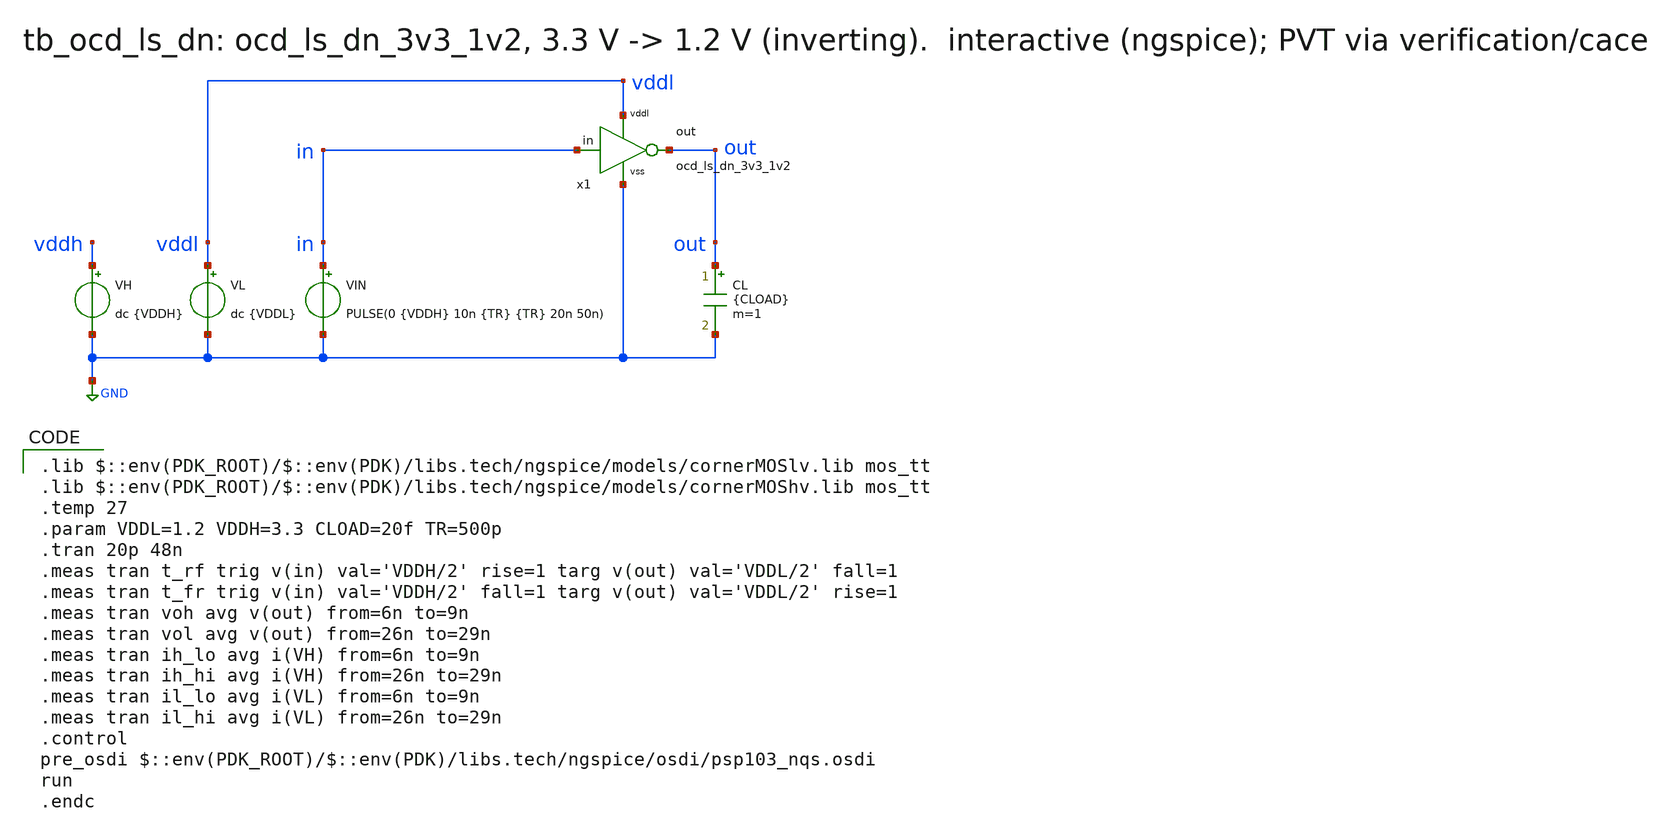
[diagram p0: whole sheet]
** sch_path: macros/ocd_ls_dn_3v3_1v2/testbenches/xschem/tb_ocd_ls_dn.sch
* macros/ocd_ls_dn_3v3_1v2/schematic/xschem/ocd_ls_dn_3v3_1v2.sym:
* Copyright 2023 IHP PDK Authors, Apache License 2.0 (https://www.apache.org/licenses/LICENSE-2.0)
**.subckt tb_ocd_ls_dn
x1 GND vddl out in ocd_ls_dn_3v3_1v2
VL vddl GND dc {VDDL}
VH vddh GND dc {VDDH}
VIN in GND PULSE(0 {VDDH} 10n {TR} {TR} 20n 50n)
CL out GND {CLOAD} m=1
**** begin user architecture code
 .lib $::env(PDK_ROOT)/$::env(PDK)/libs.tech/ngspice/models/cornerMOSlv.lib mos_tt
.lib $::env(PDK_ROOT)/$::env(PDK)/libs.tech/ngspice/models/cornerMOShv.lib mos_tt
.temp 27
.param VDDL=1.2 VDDH=3.3 CLOAD=20f TR=500p
.tran 20p 48n
.meas tran t_rf trig v(in) val='VDDH/2' rise=1 targ v(out) val='VDDL/2' fall=1
.meas tran t_fr trig v(in) val='VDDH/2' fall=1 targ v(out) val='VDDL/2' rise=1
.meas tran voh avg v(out) from=6n to=9n
.meas tran vol avg v(out) from=26n to=29n
.meas tran ih_lo avg i(VH) from=6n to=9n
.meas tran ih_hi avg i(VH) from=26n to=29n
.meas tran il_lo avg i(VL) from=6n to=9n
.meas tran il_hi avg i(VL) from=26n to=29n
.control
pre_osdi $::env(PDK_ROOT)/$::env(PDK)/libs.tech/ngspice/osdi/psp103_nqs.osdi
run
.endc
**** end user architecture code
**.ends

* expanding   symbol:  ocd_ls_dn_3v3_1v2.sym # of pins=4
** sym_path: macros/ocd_ls_dn_3v3_1v2/schematic/xschem/ocd_ls_dn_3v3_1v2.sym
** sch_path: macros/ocd_ls_dn_3v3_1v2/schematic/xschem/ocd_ls_dn_3v3_1v2.sch
.subckt ocd_ls_dn_3v3_1v2 vss vddl out in
*.iopin vss
*.iopin vddl
*.opin out
*.ipin in
XMP1 out in vddl vddl sg13_hv_pmos w=2.0u l=0.4u ng=1 m=1 mm_ok=1
XMN1 out in vss vss sg13_hv_nmos w=1.0u l=0.45u ng=1 m=1 mm_ok=1
.ends

.GLOBAL GND
.end
